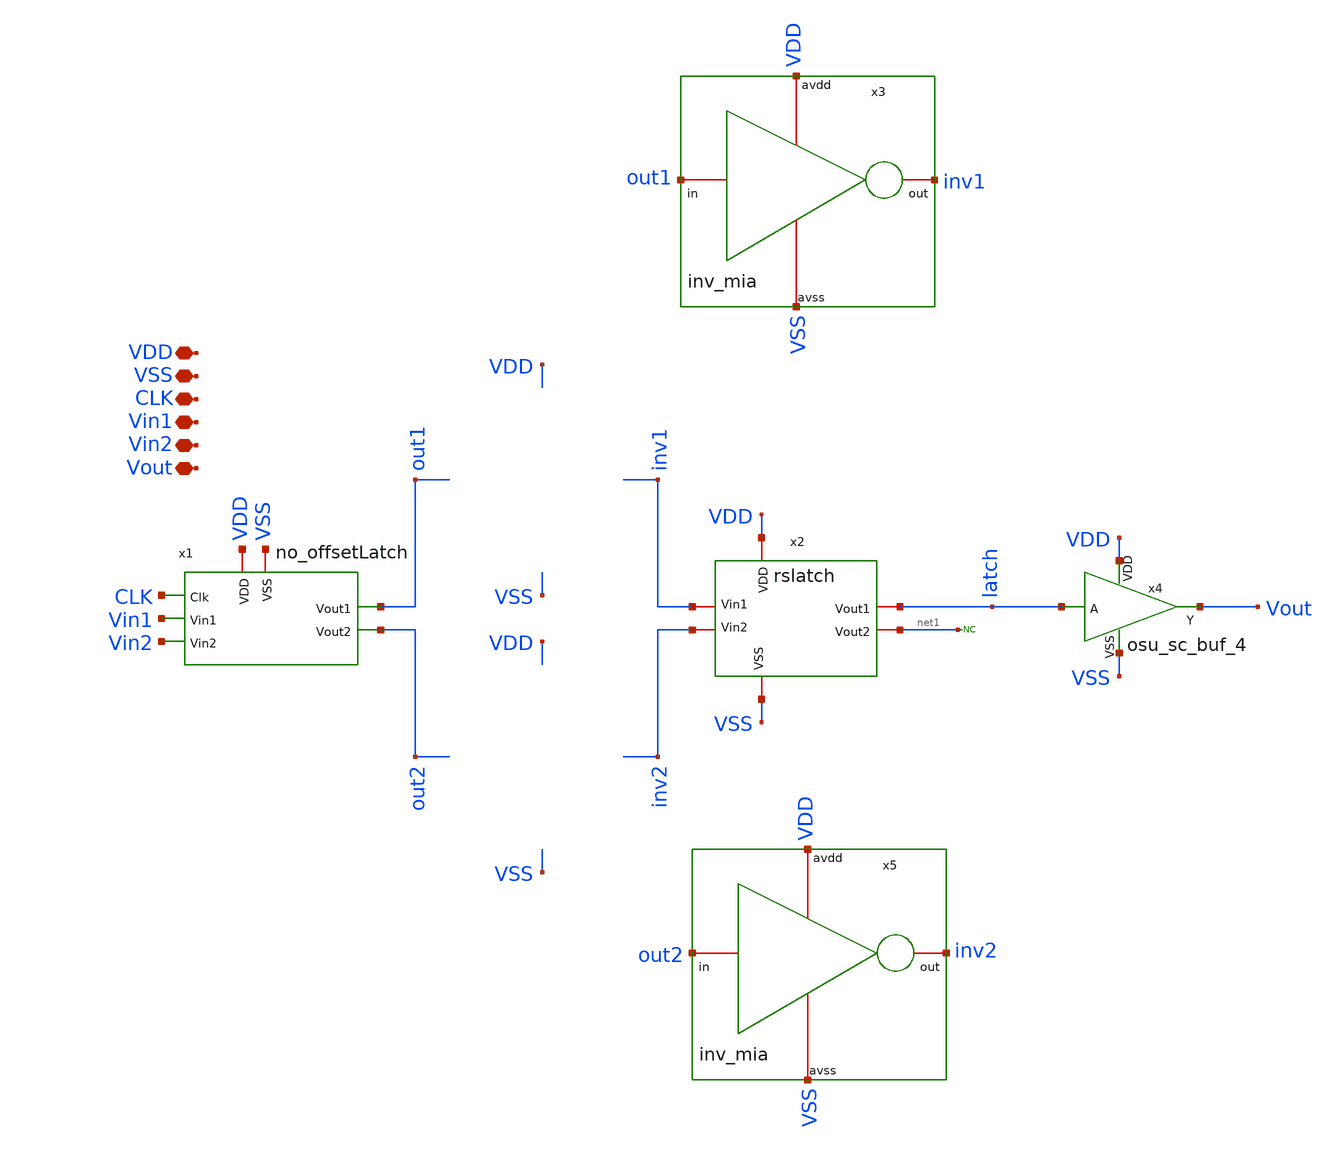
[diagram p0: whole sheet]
** sch_path: designs/FinalBlocksLayout/comparator/comparator_no_offsetcal.sch
**.subckt comparator_no_offsetcal VDD VSS CLK Vin1 Vin2 Vout
*.iopin VDD
*.iopin VSS
*.iopin CLK
*.iopin Vin1
*.iopin Vin2
*.iopin Vout
* noconn #net1
x2 VDD latch net1 inv1 inv2 VSS rslatch
x4 VDD latch Vout VSS osu_sc_buf_4
x1 CLK Vin1 Vin2 VDD VSS out1 out2 no_offsetLatch
x3 VDD out1 inv1 VSS inv_mia
x5 VDD out2 inv2 VSS inv_mia
**.ends
.end
